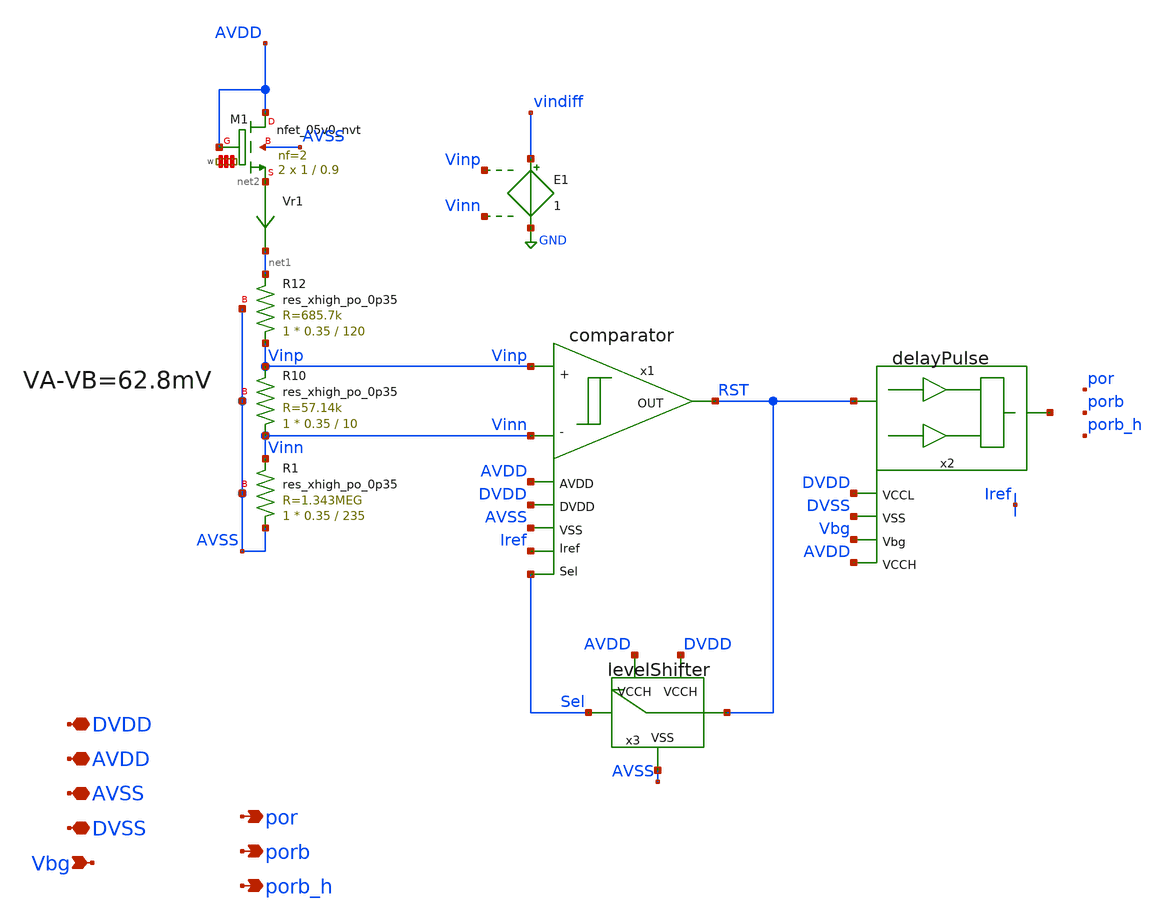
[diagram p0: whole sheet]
** sch_path: xschem/sky130_ef_ip__bgrref_por.sch
**.subckt sky130_ef_ip__bgrref_por AVDD por AVSS DVDD porb Vbg porb_h DVSS
*.iopin AVDD
*.opin por
*.iopin AVSS
*.iopin DVDD
*.opin porb
*.ipin Vbg
*.opin porb_h
*.iopin DVSS
XM1 AVDD AVDD net2 AVSS sky130_fd_pr__nfet_05v0_nvt L=0.9 W='1 * 2 ' nf=2 ad='int((nf+1)/2) * W / nf * 0.29'
+ as='int((nf+2)/2) * W / nf * 0.29' pd='2*int((nf+1)/2) * (W / nf + 0.29)' ps='2*int((nf+2)/2) * (W / nf + 0.29)'
+ nrd='0.29 / W ' nrs='0.29 / W ' sa=0 sb=0 sd=0 mult=2 m=2
Vr1 net2 net1 0
.save i(vr1)
E1 vindiff GND Vinp Vinn 1
x1 Iref Vinn Vinp RST AVSS AVDD DVDD Sel comparator
XR1 AVSS Vinn AVSS sky130_fd_pr__res_xhigh_po_0p35 L=235 mult=1 m=1
XR10 Vinn Vinp AVSS sky130_fd_pr__res_xhigh_po_0p35 L=10 mult=1 m=1
XR12 Vinp net1 AVSS sky130_fd_pr__res_xhigh_po_0p35 L=120 mult=1 m=1
x3 RST Sel DVDD AVSS AVDD levelShifter
x2 RST net3 DVDD DVSS Vbg AVDD delayPulse
**.ends
.GLOBAL GND
.end
